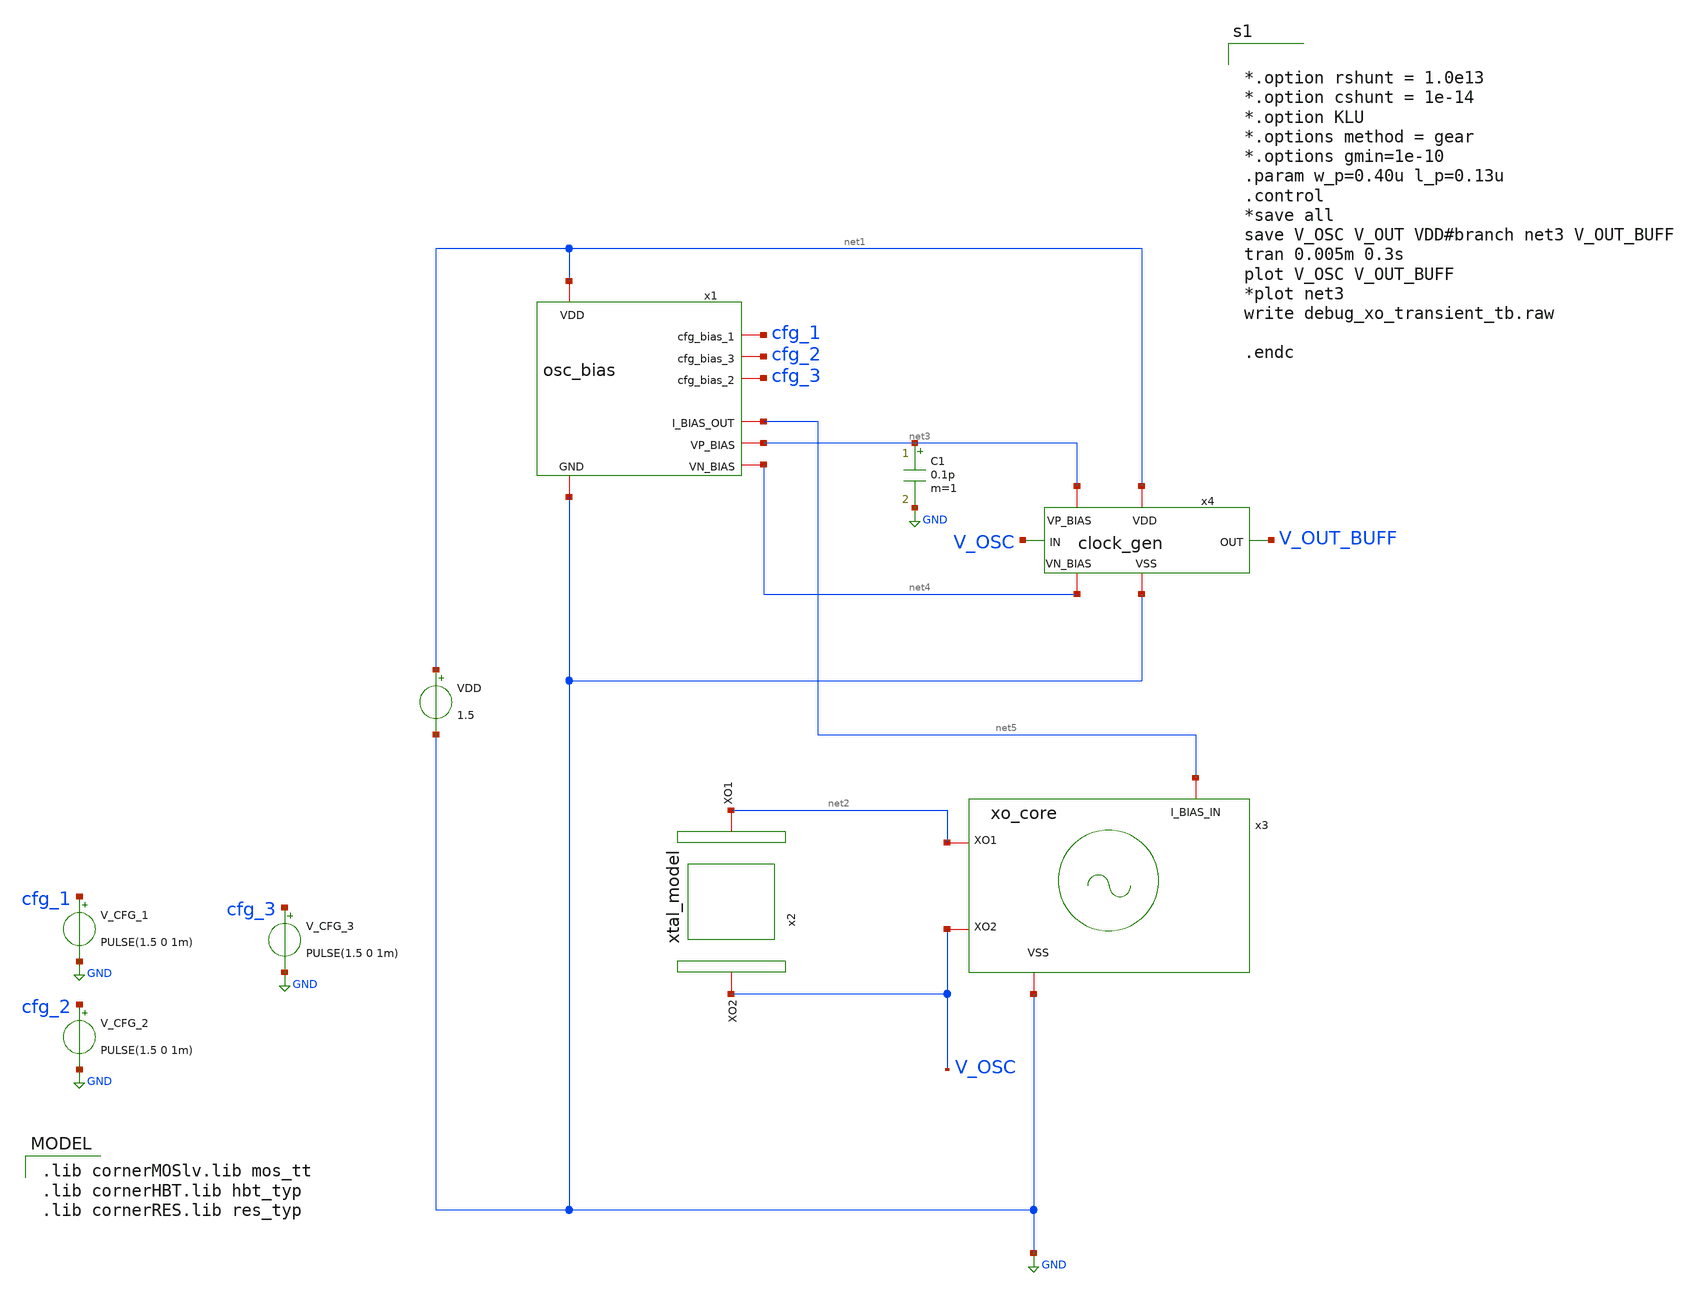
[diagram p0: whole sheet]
** sch_path: debug_xo_transient_tb.sch
**.subckt debug_xo_transient_tb
VDD net1 GND 1.5
x1 net1 cfg_1 cfg_2 cfg_3 GND net5 net3 net4 osc_bias
x2 net2 V_OSC xtal_model
x3 net5 V_OSC net2 GND xo_core
V_CFG_1 cfg_1 GND PULSE(1.5 0 1m)
V_CFG_2 cfg_2 GND PULSE(1.5 0 1m)
V_CFG_3 cfg_3 GND PULSE(1.5 0 1m)
x4 net1 V_OSC V_OUT_BUFF GND net3 net4 clock_gen
C1 net3 GND 0.1p m=1
**** begin user architecture code


*.option rshunt = 1.0e13
*.option cshunt = 1e-14
*.option KLU
*.options method = gear
*.options gmin=1e-10
.param w_p=0.40u l_p=0.13u
.control
*save all
save V_OSC V_OUT VDD#branch net3 V_OUT_BUFF
tran 0.005m 0.3s
plot V_OSC V_OUT_BUFF
*plot net3
write debug_xo_transient_tb.raw

.endc


 .lib cornerMOSlv.lib mos_tt
.lib cornerHBT.lib hbt_typ
.lib cornerRES.lib res_typ

**** end user architecture code
**.ends

* expanding   symbol:  osc_bias.sym # of pins=8
** sym_path: osc_bias.sym
** sch_path: osc_bias.sch
.subckt osc_bias VDD cfg_bias_1 cfg_bias_3 cfg_bias_2 GND I_BIAS_OUT VP_BIAS VN_BIAS
*.iopin VDD
*.iopin GND
*.iopin I_BIAS_OUT
*.iopin cfg_bias_1
*.iopin cfg_bias_2
*.iopin cfg_bias_3
*.opin VN_BIAS
*.opin VP_BIAS
XM1 VP_BIAS VP_BIAS VDD VDD sg13_lv_pmos w=0.2u l=0.13u ng=1 m=1 mm_ok=1
XM3 VP_BIAS VP_BIAS net1 GND sg13_lv_nmos w=0.2u l=10u ng=1 m=1 mm_ok=1
XM4 net1 net1 net2 GND sg13_lv_nmos w=0.2u l=10u ng=1 m=1 mm_ok=1
XM5 net2 net2 VN_BIAS GND sg13_lv_nmos w=0.2u l=10u ng=1 m=1 mm_ok=1
XM2 net6 VP_BIAS VDD VDD sg13_lv_pmos w=0.25u l=10u ng=1 m=2 mm_ok=1
XM6 I_BIAS_OUT cfg_bias_1 net6 VDD sg13_lv_pmos w=0.25u l=10u ng=1 m=1 mm_ok=1
XM7 net3 VP_BIAS VDD VDD sg13_lv_pmos w=0.25u l=10u ng=1 m=4 mm_ok=1
XM8 net4 VP_BIAS VDD VDD sg13_lv_pmos w=0.25u l=10u ng=1 m=20 mm_ok=1
XM9 I_BIAS_OUT cfg_bias_2 net3 VDD sg13_lv_pmos w=0.5u l=10u ng=1 m=1 mm_ok=1
XM10 I_BIAS_OUT cfg_bias_3 net4 VDD sg13_lv_pmos w=1u l=10u ng=1 m=1 mm_ok=1
XM11 VN_BIAS VN_BIAS net5 GND sg13_lv_nmos w=0.2u l=0.13u ng=1 m=1 mm_ok=1
Vmeas net5 GND 0
.save i(vmeas)
.ends


* expanding   symbol:  xtal_model.sym # of pins=2
** sym_path: xtal_model.sym
** sch_path: xtal_model.sch
.subckt xtal_model XO1 XO2
*.iopin XO2
*.iopin XO1
R1 XO1 net1 1k m=1
Cm net1 net2 1p m=1
C0 XO1 XO2 1p m=1
Lm net2 XO2 1n m=1
.ends


* expanding   symbol:  xo_core.sym # of pins=4
** sym_path: xo_core.sym
** sch_path: xo_core.sch
.subckt xo_core I_BIAS_IN XO2 XO1 VSS
*.iopin VSS
*.ipin I_BIAS_IN
*.iopin XO1
*.iopin XO2
XM2 net1 XO2 XO2 XO2 sg13_lv_pmos w=0.5u l=2u ng=1 m=1 mm_ok=1
XM3 net1 XO1 XO1 XO1 sg13_lv_pmos w=0.5u l=2u ng=1 m=1 mm_ok=1
XM1 XO2 XO1 VSS VSS sg13_lv_nmos w=2.0u l=0.5u ng=1 m=1 mm_ok=1
C2 XO2 VSS 8p m=1
C1 XO1 VSS 8p m=1
Vmeas I_BIAS_IN XO2 0
.save i(vmeas)
.ends


* expanding   symbol:  clock_gen.sym # of pins=6
** sym_path: clock_gen.sym
** sch_path: clock_gen.sch
.subckt clock_gen VDD IN OUT VSS VP_BIAS VN_BIAS
*.ipin IN
*.iopin VSS
*.opin OUT
*.iopin VDD
*.ipin VP_BIAS
*.ipin VN_BIAS
XM13 V_OUT_1 V_IN_1 net2 VSS sg13_lv_nmos w={w_p} l={l_p} ng=1 m=1 mm_ok=1
XM14 V_OUT_1 V_IN_1 M2_Source VDD sg13_lv_pmos w={3*{w_p}} l={l_p} ng=1 m=1 mm_ok=1
XM15 net3 VN_BIAS VSS VSS sg13_lv_nmos w={w_p} l={l_p} ng=1 m=1 mm_ok=1
XM16 net1 VP_BIAS VDD VDD sg13_lv_pmos w={3*{w_p}} l={l_p} ng=1 m=1 mm_ok=1
Vmeas_PMOS1 net1 M2_Source 0
.save i(vmeas_pmos1)
Vmeas_NMOS1 net2 net3 0
.save i(vmeas_nmos1)
C2 IN V_IN_1 110p m=1
XM17 V_OUT_2 V_OUT_1 net4 VSS sg13_lv_nmos w={w_p} l={l_p} ng=1 m=1 mm_ok=1
XM18 V_OUT_2 V_OUT_1 net6 VDD sg13_lv_pmos w={3*{w_p}} l={l_p} ng=1 m=1 mm_ok=1
Vmeas_NMOS2 net4 net7 0
.save i(vmeas_nmos2)
XM19 net5 VP_BIAS VDD VDD sg13_lv_pmos w={3*{w_p}} l={l_p} ng=1 m=1 mm_ok=1
Vmeas_PMOS2 net5 net6 0
.save i(vmeas_pmos2)
XM20 net7 VN_BIAS VSS VSS sg13_lv_nmos w={w_p} l={l_p} ng=1 m=1 mm_ok=1
XM21 OUT V_OUT_4 net9 VSS sg13_lv_nmos w={w_p} l={l_p} ng=1 m=1 mm_ok=1
XM22 OUT V_OUT_4 net8 VDD sg13_lv_pmos w={3*{w_p}} l={l_p} ng=1 m=1 mm_ok=1
Vmeas_PMOS_OUT VDD net8 0
.save i(vmeas_pmos_out)
Vmeas_NMOS_OUT net9 VSS 0
.save i(vmeas_nmos_out)
XM25 V_OUT_3 V_OUT_2 net10 VSS sg13_lv_nmos w={w_p} l={l_p} ng=1 m=1 mm_ok=1
XM26 V_OUT_3 V_OUT_2 net12 VDD sg13_lv_pmos w={3*{w_p}} l={l_p} ng=1 m=1 mm_ok=1
Vmeas_NMOS3 net10 net13 0
.save i(vmeas_nmos3)
XM27 net11 VP_BIAS VDD VDD sg13_lv_pmos w={3*{w_p}} l={l_p} ng=1 m=1 mm_ok=1
Vmeas_PMOS3 net11 net12 0
.save i(vmeas_pmos3)
XM28 net13 VN_BIAS VSS VSS sg13_lv_nmos w={w_p} l={l_p} ng=1 m=1 mm_ok=1
XM29 V_OUT_4 V_OUT_3 net14 VSS sg13_lv_nmos w={w_p} l={l_p} ng=1 m=1 mm_ok=1
XM30 V_OUT_4 V_OUT_3 net16 VDD sg13_lv_pmos w={3*{w_p}} l={l_p} ng=1 m=1 mm_ok=1
Vmeas_NMOS4 net14 net17 0
.save i(vmeas_nmos4)
XM31 net15 VP_BIAS VDD VDD sg13_lv_pmos w={3*{w_p}} l={l_p} ng=1 m=1 mm_ok=1
Vmeas_PMOS4 net15 net16 0
.save i(vmeas_pmos4)
XM32 net17 VN_BIAS VSS VSS sg13_lv_nmos w={w_p} l={l_p} ng=1 m=1 mm_ok=1
XM1 net18 V_OUT_1 V_OUT_1 V_OUT_1 sg13_lv_pmos w=0.5u l=2u ng=1 m=1 mm_ok=1
XM2 net18 V_IN_1 V_IN_1 V_IN_1 sg13_lv_pmos w=0.5u l=2u ng=1 m=1 mm_ok=1
.ends

.GLOBAL GND
.end
